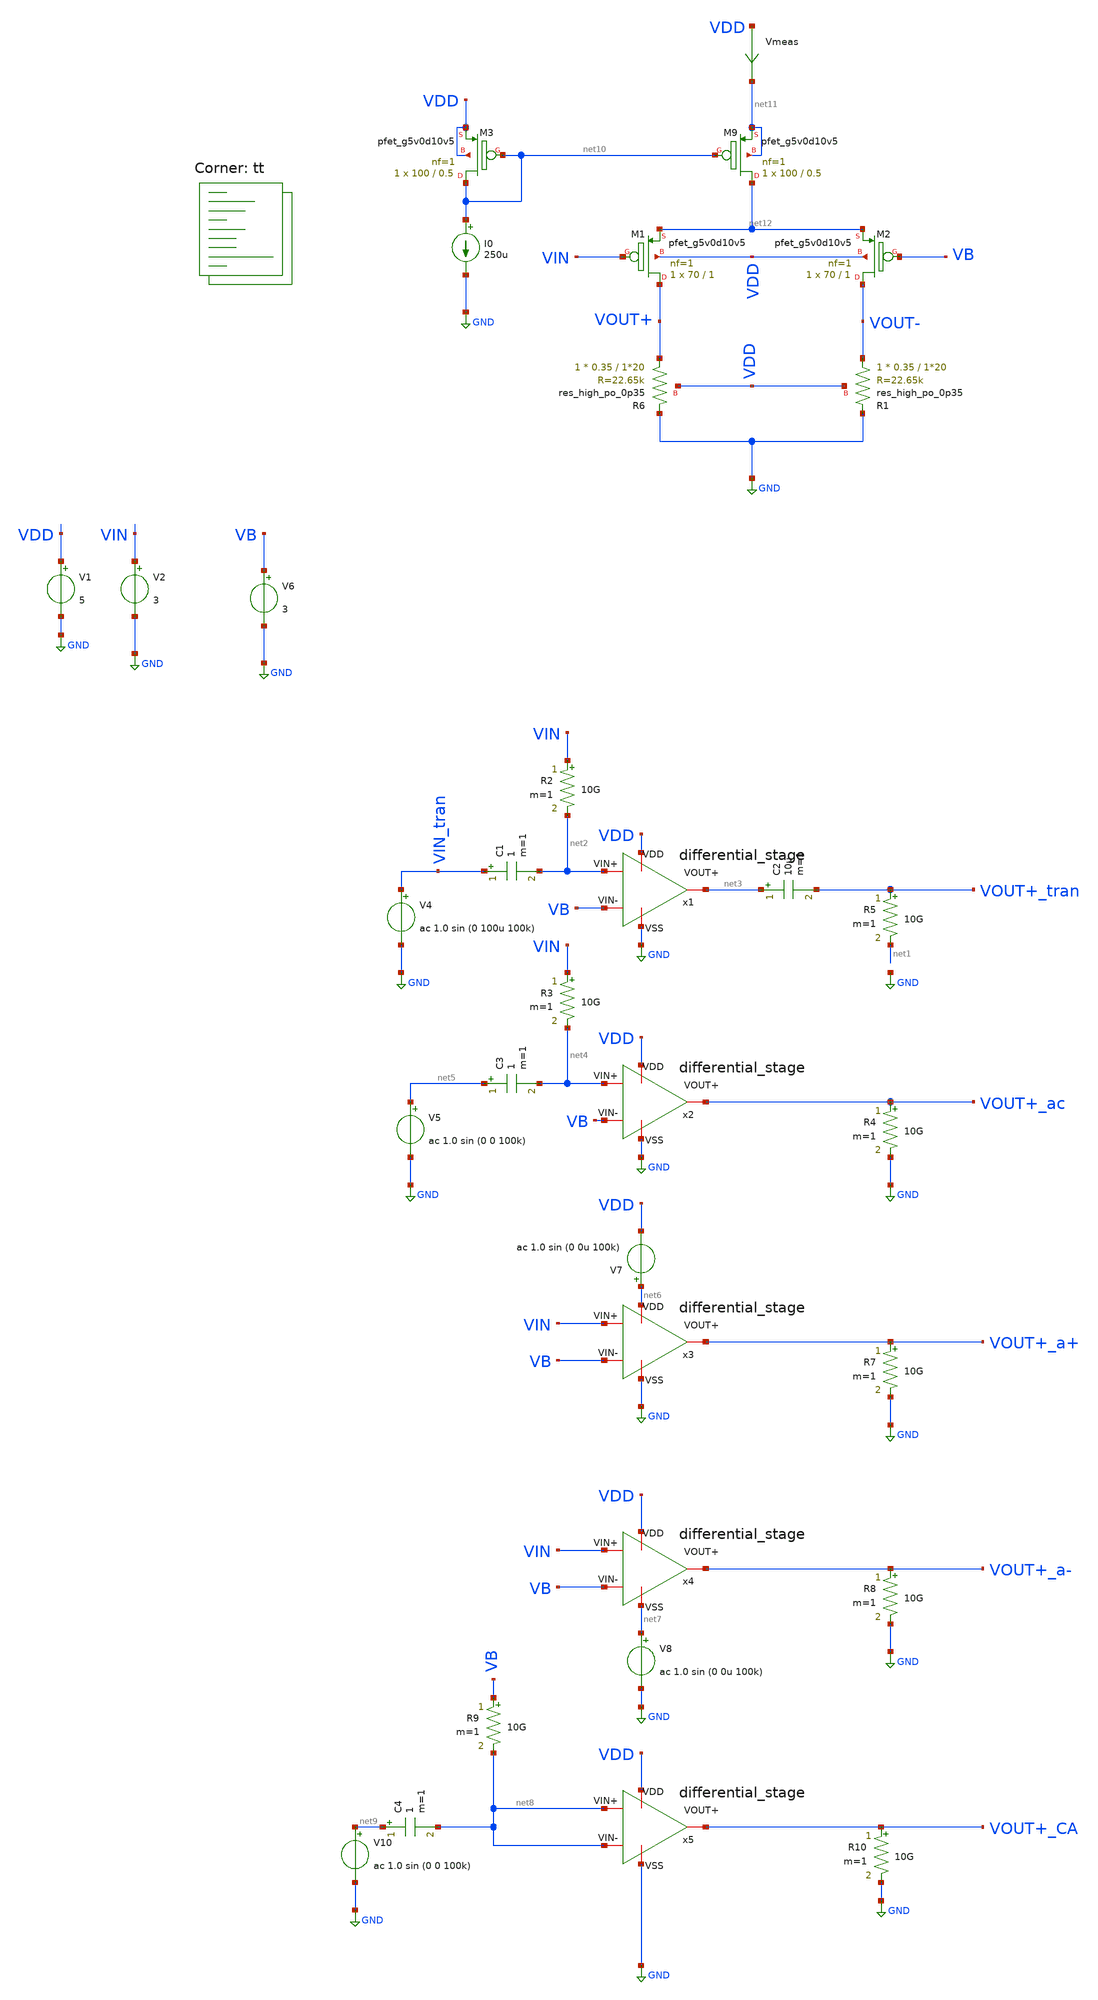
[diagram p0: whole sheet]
** sch_path: amplifiers/differencial_stage_amps/basic_stages/basic_PMOS_resistive_stage/diferential_stage.sch
**.subckt diferential_stage
V1 VDD GND 5
V2 VIN GND 3
V6 VB GND 3
R5 VOUT+_tran net1 10G m=1
R2 VIN net2 10G m=1
V4 VIN_tran GND ac 1.0 sin (0 100u 100k)
C2 net3 VOUT+_tran 10u m=1
C1 VIN_tran net2 1 m=1
R3 VIN net4 10G m=1
C3 net5 net4 1 m=1
V5 net5 GND ac 1.0 sin (0 0 100k)
R4 VOUT+_ac GND 10G m=1
V7 net6 VDD ac 1.0 sin (0 0u 100k)
R7 VOUT+_a+ GND 10G m=1
V8 net7 GND ac 1.0 sin (0 0u 100k)
R8 VOUT+_a- GND 10G m=1
R9 VB net8 10G m=1
C4 net9 net8 1 m=1
V10 net9 GND ac 1.0 sin (0 0 100k)
XM9 net12 net10 net11 net11 sky130_fd_pr__pfet_g5v0d10v5 L=0.5 W=100 nf=1 ad='int((1 + 1)/2) * 100 / 1 * 0.29'
+ as='int((1 + 2)/2) * 100 / 1 * 0.29' pd='2*int((1 + 1)/2) * (100 / 1 + 0.29)' ps='2*int((1 + 2)/2) * (100 / 1 + 0.29)'
+ nrd='0.29 / 100 ' nrs='0.29 / 100 ' sa=0 sb=0 sd=0 mult=1 m=1
XM1 VOUT+ VIN net12 VDD sky130_fd_pr__pfet_g5v0d10v5 L=1 W=70 nf=1 ad='int((1 + 1)/2) * 70 / 1 * 0.29'
+ as='int((1 + 2)/2) * 70 / 1 * 0.29' pd='2*int((1 + 1)/2) * (70 / 1 + 0.29)' ps='2*int((1 + 2)/2) * (70 / 1 + 0.29)'
+ nrd='0.29 / 70 ' nrs='0.29 / 70 ' sa=0 sb=0 sd=0 mult=1 m=1
XM2 VOUT- VB net12 VDD sky130_fd_pr__pfet_g5v0d10v5 L=1 W=70 nf=1 ad='int((1 + 1)/2) * 70 / 1 * 0.29'
+ as='int((1 + 2)/2) * 70 / 1 * 0.29' pd='2*int((1 + 1)/2) * (70 / 1 + 0.29)' ps='2*int((1 + 2)/2) * (70 / 1 + 0.29)'
+ nrd='0.29 / 70 ' nrs='0.29 / 70 ' sa=0 sb=0 sd=0 mult=1 m=1
XR6 VOUT+ GND VDD sky130_fd_pr__res_high_po_0p35 L=1*20 mult=1 m=1
XR1 VOUT- GND VDD sky130_fd_pr__res_high_po_0p35 L=1*20 mult=1 m=1
XM3 net10 net10 VDD VDD sky130_fd_pr__pfet_g5v0d10v5 L=0.5 W=100 nf=1 ad='int((1 + 1)/2) * 100 / 1 * 0.29'
+ as='int((1 + 2)/2) * 100 / 1 * 0.29' pd='2*int((1 + 1)/2) * (100 / 1 + 0.29)' ps='2*int((1 + 2)/2) * (100 / 1 + 0.29)'
+ nrd='0.29 / 100 ' nrs='0.29 / 100 ' sa=0 sb=0 sd=0 mult=1 m=1
I0 net10 GND 250u
Vmeas VDD net11 0
.save i(vmeas)
x1 VDD GND net2 VB net3 differential_stage
x2 VDD GND net4 VB VOUT+_ac differential_stage
x3 net6 GND VIN VB VOUT+_a+ differential_stage
x4 VDD net7 VIN VB VOUT+_a- differential_stage
x5 VDD GND net8 net8 VOUT+_CA differential_stage
R10 VOUT+_CA GND 10G m=1
**** begin user architecture code

**************************************************************
**************************************************************
**************************************************************
**************************************************************
**************************************************************
*LIBs*********************************************************
**************************************************************
**************************************************************
**************************************************************
**************************************************************
**************************************************************
*.lib $::SKYWATER_MODELS/sky130.lib.spice tt
* chose the corners in the corner file
* tt_mm for mismatch
* ss ff sf fs standart corners
* ll hh lh hl capacitor and resistors corners
* mc for total process variation including corners
**************************************************************
**************************************************************
**************************************************************
**************************************************************
**************************************************************
*Corners/montecarlo options***********************************
**************************************************************
**************************************************************
**************************************************************
**************************************************************
**************************************************************
.TEMP 27
**************************************************************
**************************************************************
**************************************************************
**************************************************************
*SIMULATION and Plots*****************************************
**************************************************************
**************************************************************
**************************************************************
**************************************************************
.control
save all
dc V2 0 5 0.01
*dc simulation
plot v(VOUT-) v(VIN) deriv(v(VOUT-)) v(VOUT+) deriv(v(VOUT+))
*ploting VIN VOUT and the voltage gain
plot i(Vmeas)
*ploting the current for curiosity
tran 0.1ns 20u
*transient simulation
plot (v(VOUT+_tran)) v(VIN_tran)
*simple plot to exemplify the gain
fft v(VOUT+_tran) v(VIN_tran)
*fast fourier transfor
plot mag(v(VOUT+_tran)) mag(v(VIN_tran))
ac dec 20 1 1000G
*simple ac simulation
plot db(v(VOUT+_ac))
plot db(v(VOUT+_a+))
plot db(v(VOUT+_a-))
plot db(v(VOUT+_CA))
plot db((v(VOUT+_ac))/(v(VOUT+_CA)))
plot db((v(VOUT+_ac))/(v(VOUT+_a+)))
plot db((v(VOUT+_ac))/(v(VOUT+_a-)))
.endc

.lib $::SKYWATER_MODELS/sky130.lib.spice tt
**** end user architecture code
**.ends
.GLOBAL GND
.end
